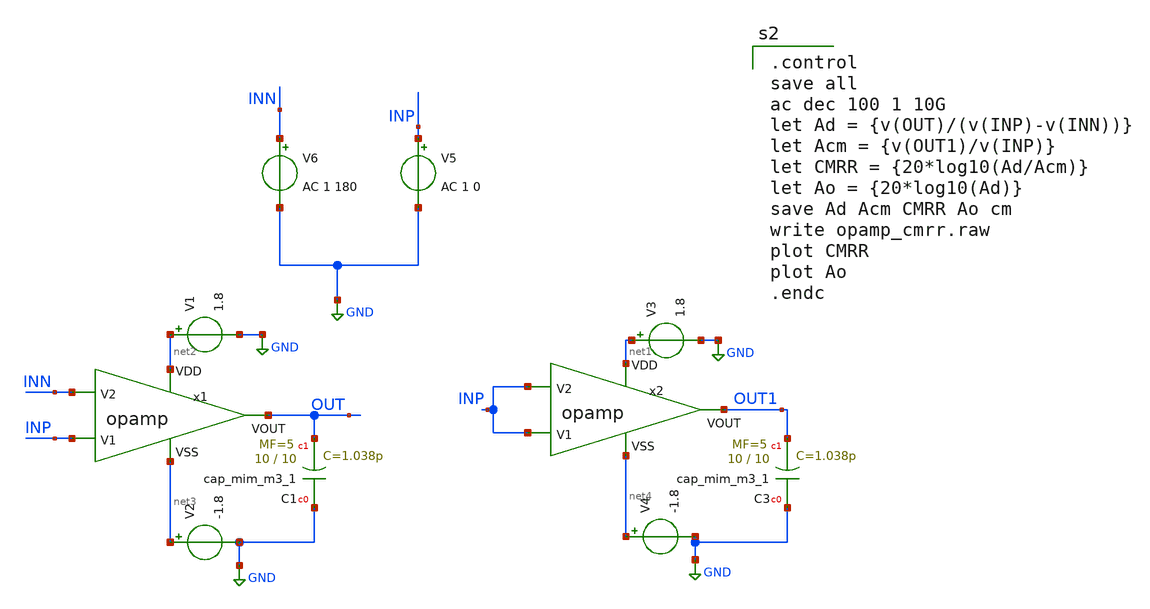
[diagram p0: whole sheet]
** sch_path: opamp_cmrr.sch
**.subckt opamp_cmrr
V6 INN GND AC 1 180
V5 INP GND AC 1 0
V1 net2 GND 1.8
V2 net3 GND -1.8
V3 net1 GND 1.8
V4 net4 GND -1.8
x1 net2 net3 INP INN OUT opamp
x2 net1 net4 INP INP OUT1 opamp
XC3 GND OUT1 sky130_fd_pr__cap_mim_m3_1 W=10 L=10 MF=5 m=5
XC1 GND OUT sky130_fd_pr__cap_mim_m3_1 W=10 L=10 MF=5 m=5
**** begin user architecture code

.control
save all
ac dec 100 1 10G
let Ad = {v(OUT)/(v(INP)-v(INN))}
let Acm = {v(OUT1)/v(INP)}
let CMRR = {20*log10(Ad/Acm)}
let Ao = {20*log10(Ad)}
save Ad Acm CMRR Ao cm
write opamp_cmrr.raw
plot CMRR
plot Ao
.endc


** opencircuitdesign pdks install
.lib $::SKYWATER_MODELS/sky130.lib.spice tt


**** end user architecture code
**.ends

* expanding   symbol:  ../xschem/opamp.sym # of pins=5
** sym_path: ../xschem/opamp.sym
** sch_path: ../xschem/opamp.sch
.subckt opamp VDD VSS V1 V2 VOUT
*.ipin VSS
*.ipin VDD
*.ipin V2
*.ipin V1
*.opin VOUT
XM2 net2 V2 net1 VSS sky130_fd_pr__nfet_g5v0d10v5 L=1 W=17.45 nf=1 ad='int((nf+1)/2) * W/nf * 0.29' as='int((nf+2)/2) * W/nf * 0.29'
+ pd='2*int((nf+1)/2) * (W/nf + 0.29)' ps='2*int((nf+2)/2) * (W/nf + 0.29)' nrd='0.29 / W' nrs='0.29 / W'
+ sa=0 sb=0 sd=0 mult=1 m=1
XM1 net3 net2 VDD VDD sky130_fd_pr__pfet_g5v0d10v5 L=1 W=30 nf=1 ad='int((nf+1)/2) * W/nf * 0.29' as='int((nf+2)/2) * W/nf * 0.29'
+ pd='2*int((nf+1)/2) * (W/nf + 0.29)' ps='2*int((nf+2)/2) * (W/nf + 0.29)' nrd='0.29 / W' nrs='0.29 / W'
+ sa=0 sb=0 sd=0 mult=1 m=1
XM4 net3 V1 net1 VSS sky130_fd_pr__nfet_g5v0d10v5 L=1 W=17.45 nf=1 ad='int((nf+1)/2) * W/nf * 0.29' as='int((nf+2)/2) * W/nf * 0.29'
+ pd='2*int((nf+1)/2) * (W/nf + 0.29)' ps='2*int((nf+2)/2) * (W/nf + 0.29)' nrd='0.29 / W' nrs='0.29 / W'
+ sa=0 sb=0 sd=0 mult=1 m=1
XM5 net6 net4 VSS VSS sky130_fd_pr__nfet_g5v0d10v5 L=1 W=15.17 nf=1 ad='int((nf+1)/2) * W/nf * 0.29'
+ as='int((nf+2)/2) * W/nf * 0.29' pd='2*int((nf+1)/2) * (W/nf + 0.29)' ps='2*int((nf+2)/2) * (W/nf + 0.29)'
+ nrd='0.29 / W' nrs='0.29 / W' sa=0 sb=0 sd=0 mult=1 m=1
XM6 net8 net4 VSS VSS sky130_fd_pr__nfet_g5v0d10v5 L=1 W=19 nf=1 ad='int((nf+1)/2) * W/nf * 0.29' as='int((nf+2)/2) * W/nf * 0.29'
+ pd='2*int((nf+1)/2) * (W/nf + 0.29)' ps='2*int((nf+2)/2) * (W/nf + 0.29)' nrd='0.29 / W' nrs='0.29 / W'
+ sa=0 sb=0 sd=0 mult=1 m=1
XM7 net4 net4 VSS VSS sky130_fd_pr__nfet_g5v0d10v5 L=1 W=15.17 nf=1 ad='int((nf+1)/2) * W/nf * 0.29'
+ as='int((nf+2)/2) * W/nf * 0.29' pd='2*int((nf+1)/2) * (W/nf + 0.29)' ps='2*int((nf+2)/2) * (W/nf + 0.29)'
+ nrd='0.29 / W' nrs='0.29 / W' sa=0 sb=0 sd=0 mult=1 m=1
XM3 net2 net2 VDD VDD sky130_fd_pr__pfet_g5v0d10v5 L=1 W=30 nf=1 ad='int((nf+1)/2) * W/nf * 0.29' as='int((nf+2)/2) * W/nf * 0.29'
+ pd='2*int((nf+1)/2) * (W/nf + 0.29)' ps='2*int((nf+2)/2) * (W/nf + 0.29)' nrd='0.29 / W' nrs='0.29 / W'
+ sa=0 sb=0 sd=0 mult=1 m=1
XM8 VOUT net3 VDD VDD sky130_fd_pr__pfet_g5v0d10v5 L=1 W=38 nf=1 ad='int((nf+1)/2) * W/nf * 0.29' as='int((nf+2)/2) * W/nf * 0.29'
+ pd='2*int((nf+1)/2) * (W/nf + 0.29)' ps='2*int((nf+2)/2) * (W/nf + 0.29)' nrd='0.29 / W' nrs='0.29 / W'
+ sa=0 sb=0 sd=0 mult=2 m=2
XC1 net5 net3 sky130_fd_pr__cap_mim_m3_1 W=9 L=9 MF=2 m=2
V_ibias net7 net4 0
.save i(v_ibias)
XR3 net5 VOUT VSS sky130_fd_pr__res_high_po_0p69 L=3.2 mult=1 m=1
V_ibias1 net1 net6 0
.save i(v_ibias1)
I1 net9 net10 63.26u
V_iout VOUT net8 0
.save i(v_iout)
XM9 VDD VDD net7 VSS sky130_fd_pr__nfet_g5v0d10v5 L=1 W=0.69 nf=1 ad='int((nf+1)/2) * W/nf * 0.29' as='int((nf+2)/2) * W/nf * 0.29'
+ pd='2*int((nf+1)/2) * (W/nf + 0.29)' ps='2*int((nf+2)/2) * (W/nf + 0.29)' nrd='0.29 / W' nrs='0.29 / W'
+ sa=0 sb=0 sd=0 mult=1 m=1
.ends

.GLOBAL GND
.end
